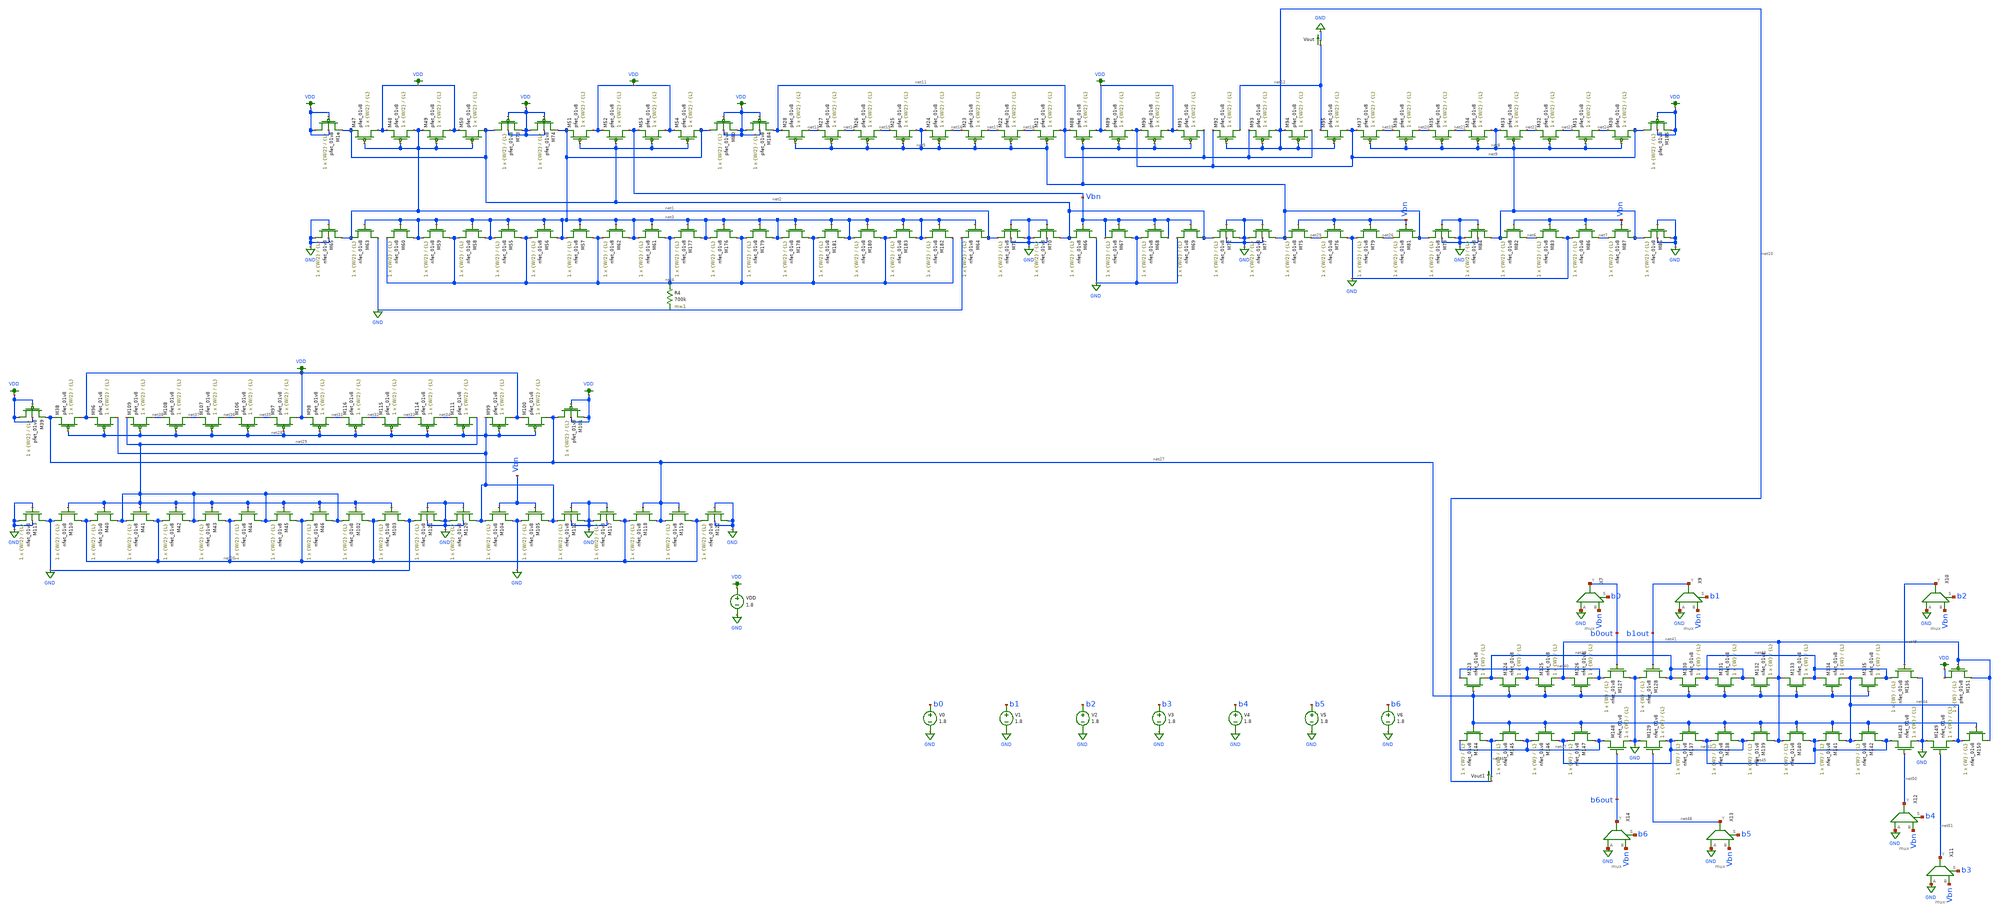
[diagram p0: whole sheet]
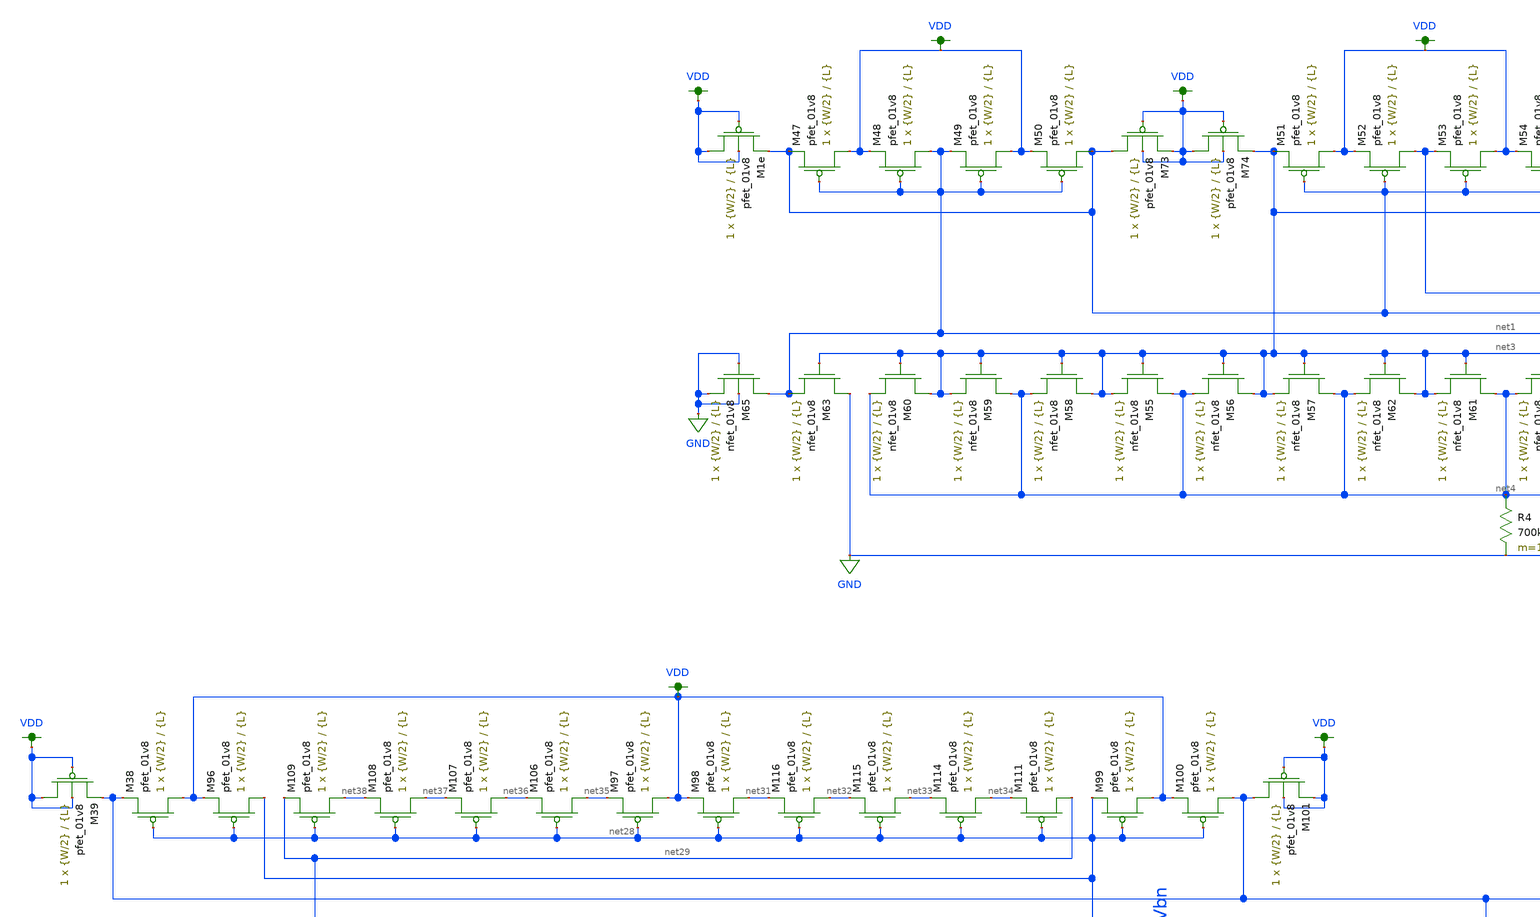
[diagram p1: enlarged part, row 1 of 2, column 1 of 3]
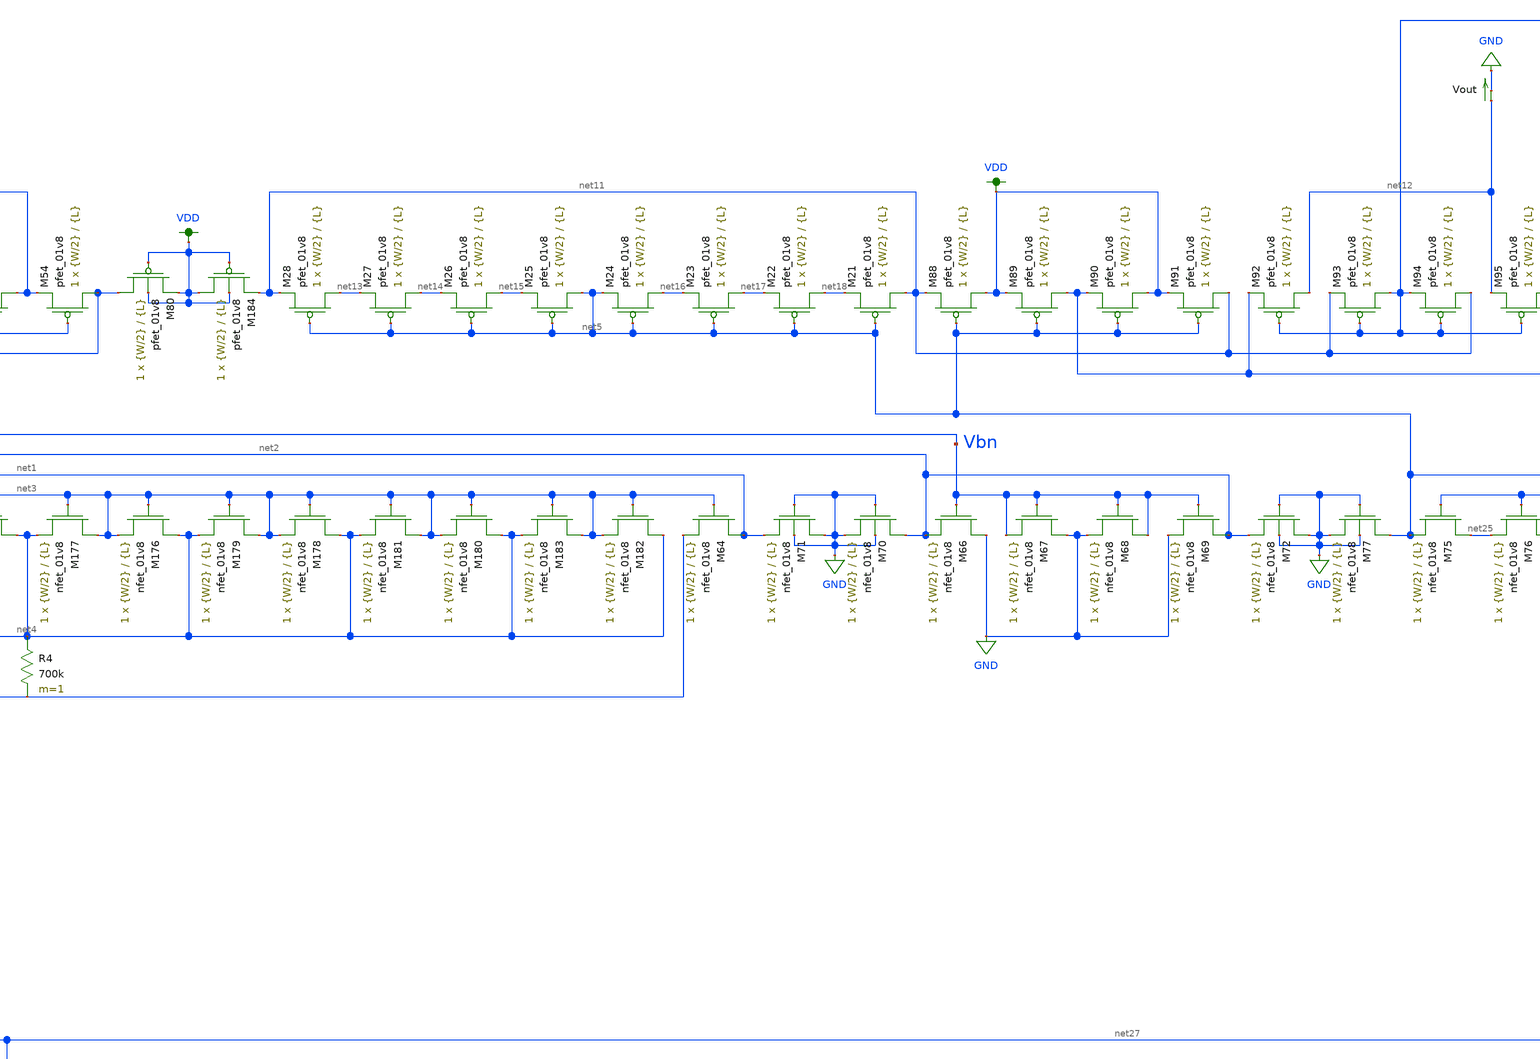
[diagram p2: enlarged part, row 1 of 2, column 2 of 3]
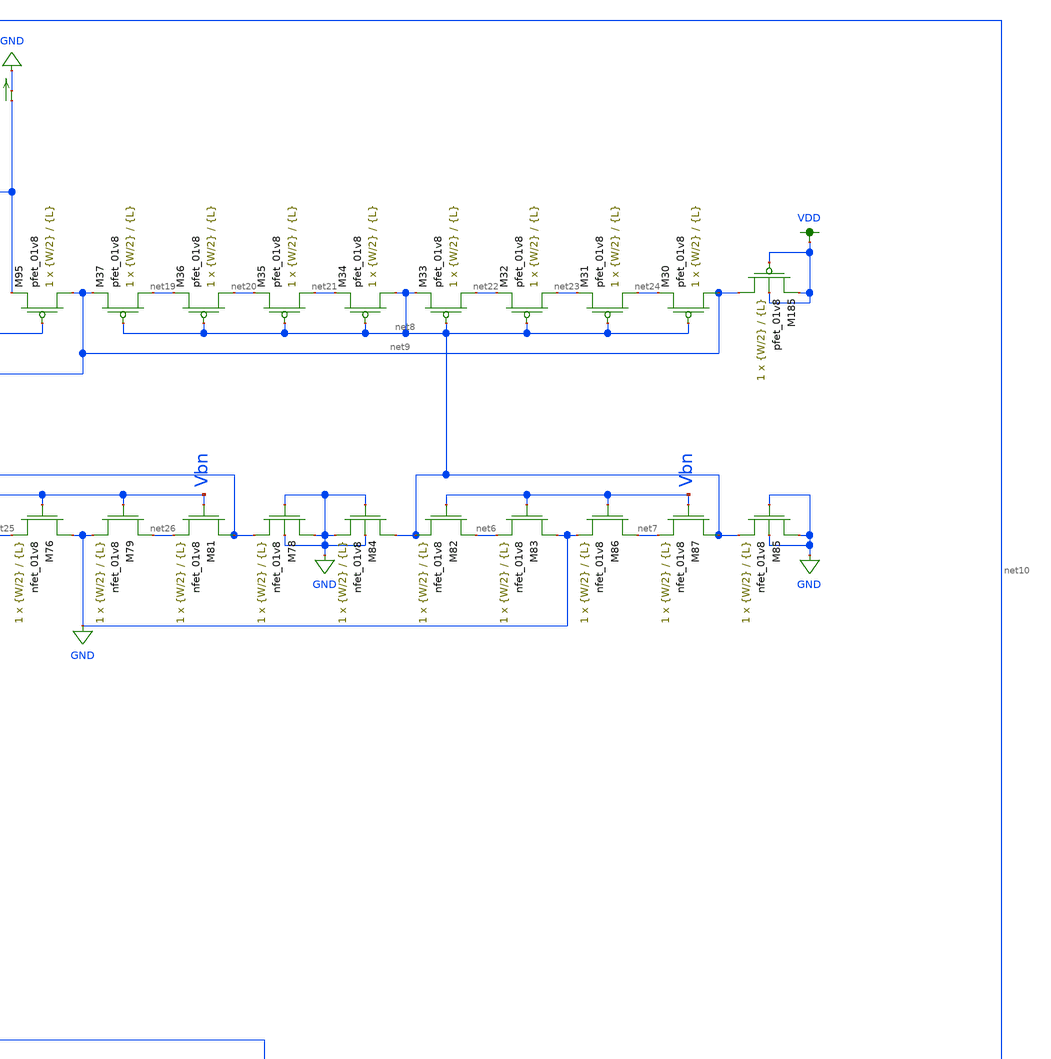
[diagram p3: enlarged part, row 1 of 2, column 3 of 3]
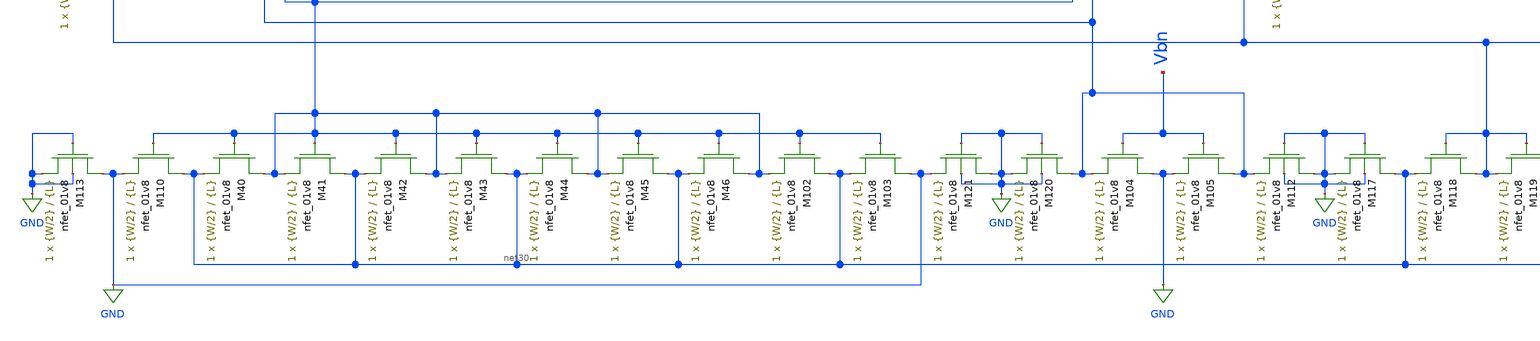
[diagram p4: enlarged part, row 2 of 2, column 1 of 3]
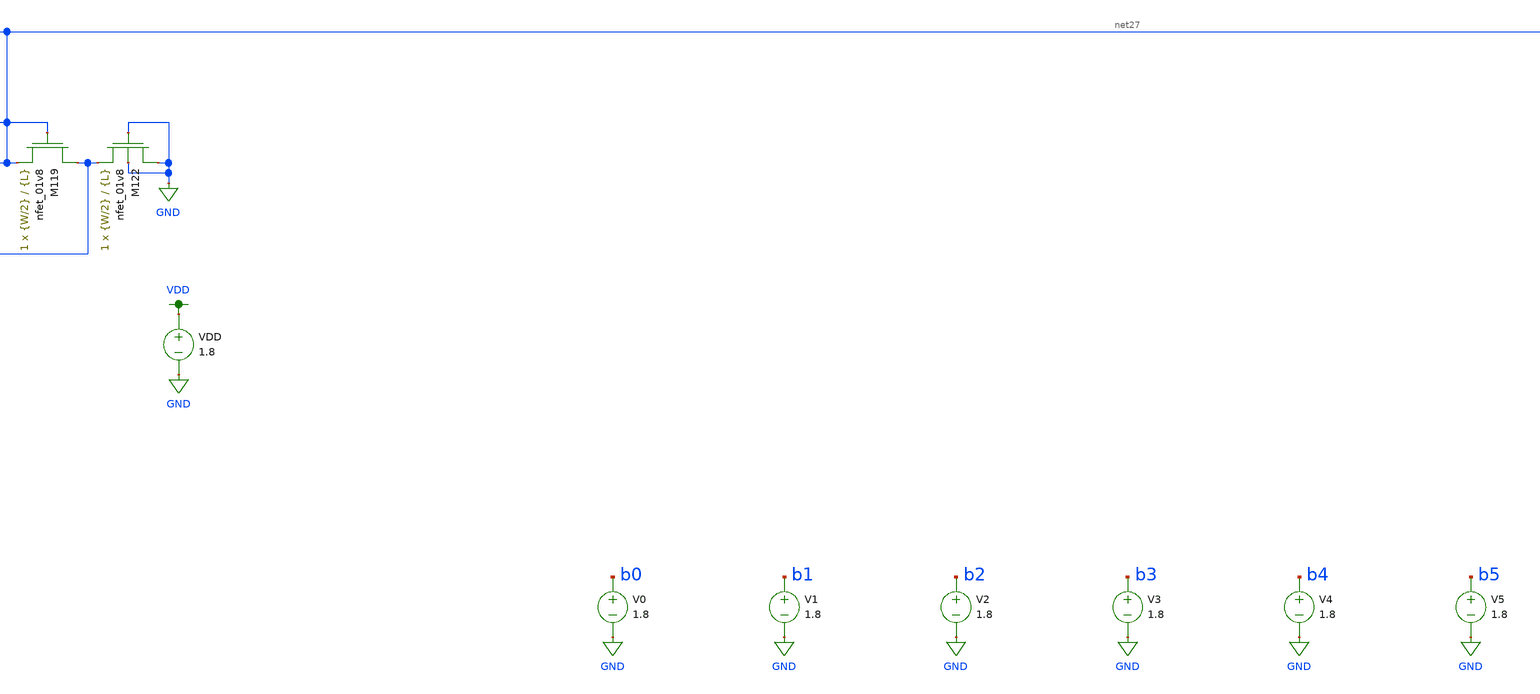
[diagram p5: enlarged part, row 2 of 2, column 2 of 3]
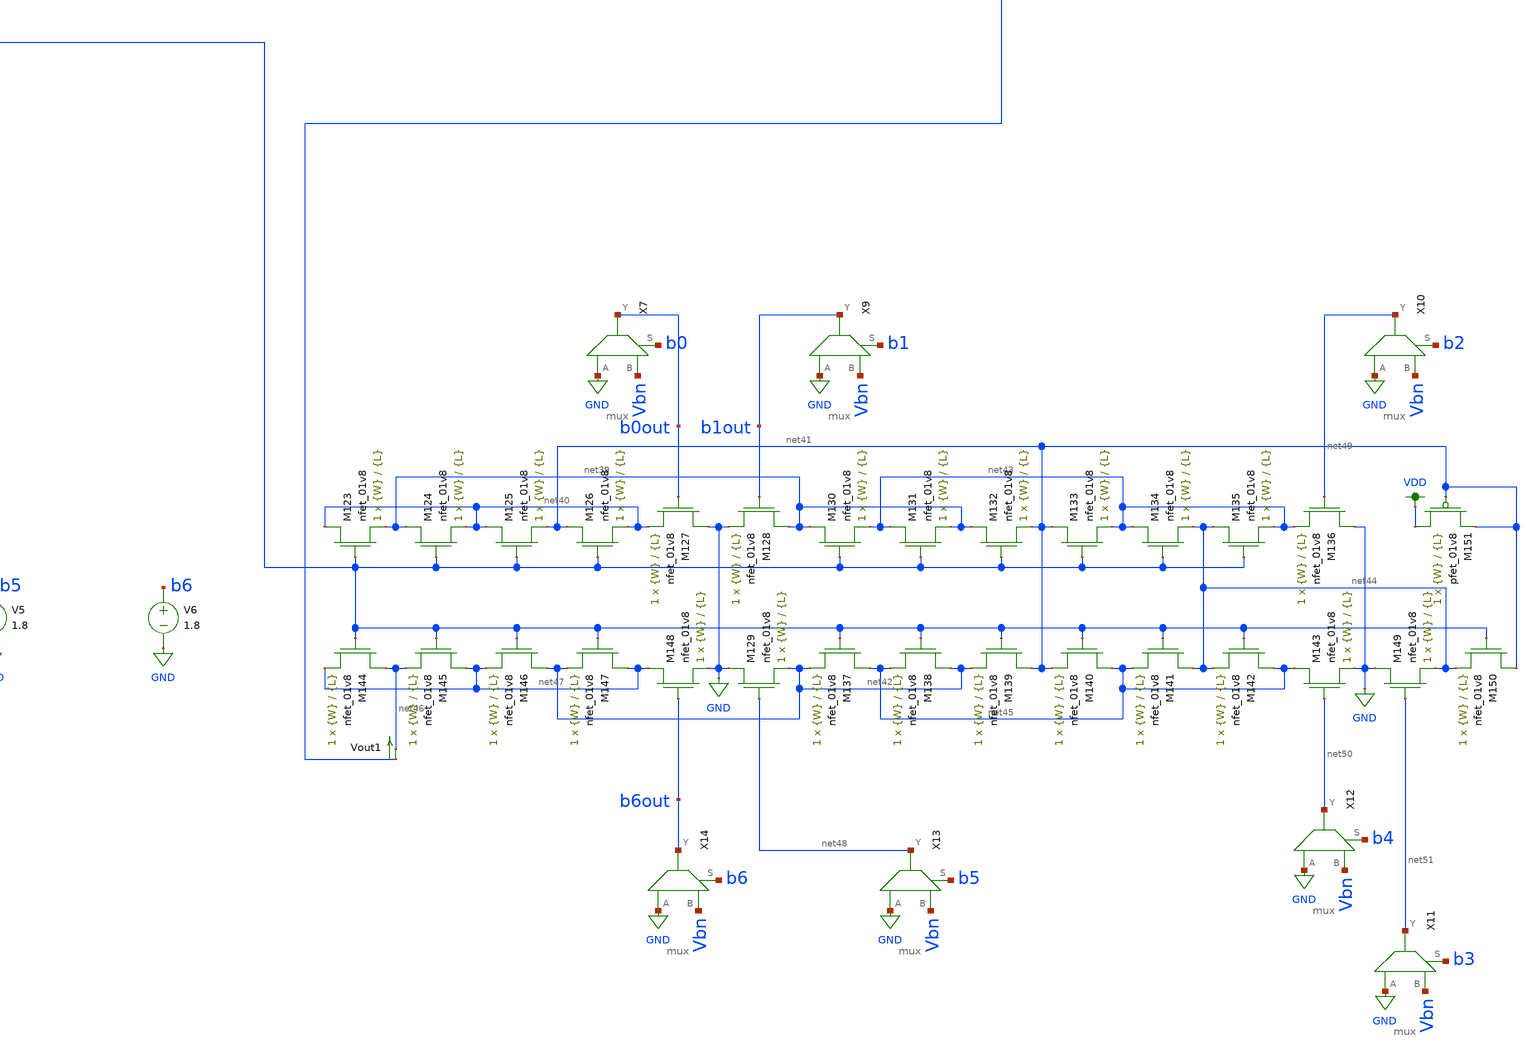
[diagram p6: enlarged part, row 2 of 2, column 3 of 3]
** sch_path: schematics/dac_dnl_inl_current_mirror_lds.sch
**.subckt dac_dnl_inl_current_mirror_lds
V0 b0 GND 1.8
V1 b1 GND 1.8
V2 b2 GND 1.8
V3 b3 GND 1.8
V4 b4 GND 1.8
V5 b5 GND 1.8
V6 b6 GND 1.8
VDD VDD GND 1.8
XM47 VDD net1 net2 VDD sky130_fd_pr__pfet_01v8 L={L} W={W/2} nf=1 ad='int((nf+1)/2) * W/nf * 0.29' as='int((nf+2)/2) * W/nf * 0.29'
+ pd='2*int((nf+1)/2) * (W/nf + 0.29)' ps='2*int((nf+2)/2) * (W/nf + 0.29)' nrd='0.29 / W' nrs='0.29 / W'
+ sa=0 sb=0 sd=0 mult=1 m=1
XM48 net1 net1 VDD VDD sky130_fd_pr__pfet_01v8 L={L} W={W/2} nf=1 ad='int((nf+1)/2) * W/nf * 0.29' as='int((nf+2)/2) * W/nf * 0.29'
+ pd='2*int((nf+1)/2) * (W/nf + 0.29)' ps='2*int((nf+2)/2) * (W/nf + 0.29)' nrd='0.29 / W' nrs='0.29 / W'
+ sa=0 sb=0 sd=0 mult=1 m=1
XM49 VDD net1 net1 VDD sky130_fd_pr__pfet_01v8 L={L} W={W/2} nf=1 ad='int((nf+1)/2) * W/nf * 0.29' as='int((nf+2)/2) * W/nf * 0.29'
+ pd='2*int((nf+1)/2) * (W/nf + 0.29)' ps='2*int((nf+2)/2) * (W/nf + 0.29)' nrd='0.29 / W' nrs='0.29 / W'
+ sa=0 sb=0 sd=0 mult=1 m=1
XM50 net2 net1 VDD VDD sky130_fd_pr__pfet_01v8 L={L} W={W/2} nf=1 ad='int((nf+1)/2) * W/nf * 0.29' as='int((nf+2)/2) * W/nf * 0.29'
+ pd='2*int((nf+1)/2) * (W/nf + 0.29)' ps='2*int((nf+2)/2) * (W/nf + 0.29)' nrd='0.29 / W' nrs='0.29 / W'
+ sa=0 sb=0 sd=0 mult=1 m=1
XM51 VDD net2 net3 VDD sky130_fd_pr__pfet_01v8 L={L} W={W/2} nf=1 ad='int((nf+1)/2) * W/nf * 0.29' as='int((nf+2)/2) * W/nf * 0.29'
+ pd='2*int((nf+1)/2) * (W/nf + 0.29)' ps='2*int((nf+2)/2) * (W/nf + 0.29)' nrd='0.29 / W' nrs='0.29 / W'
+ sa=0 sb=0 sd=0 mult=1 m=1
XM52 Vbn net2 VDD VDD sky130_fd_pr__pfet_01v8 L={L} W={W/2} nf=1 ad='int((nf+1)/2) * W/nf * 0.29' as='int((nf+2)/2) * W/nf * 0.29'
+ pd='2*int((nf+1)/2) * (W/nf + 0.29)' ps='2*int((nf+2)/2) * (W/nf + 0.29)' nrd='0.29 / W' nrs='0.29 / W'
+ sa=0 sb=0 sd=0 mult=1 m=1
XM53 VDD net2 Vbn VDD sky130_fd_pr__pfet_01v8 L={L} W={W/2} nf=1 ad='int((nf+1)/2) * W/nf * 0.29' as='int((nf+2)/2) * W/nf * 0.29'
+ pd='2*int((nf+1)/2) * (W/nf + 0.29)' ps='2*int((nf+2)/2) * (W/nf + 0.29)' nrd='0.29 / W' nrs='0.29 / W'
+ sa=0 sb=0 sd=0 mult=1 m=1
XM54 net3 net2 VDD VDD sky130_fd_pr__pfet_01v8 L={L} W={W/2} nf=1 ad='int((nf+1)/2) * W/nf * 0.29' as='int((nf+2)/2) * W/nf * 0.29'
+ pd='2*int((nf+1)/2) * (W/nf + 0.29)' ps='2*int((nf+2)/2) * (W/nf + 0.29)' nrd='0.29 / W' nrs='0.29 / W'
+ sa=0 sb=0 sd=0 mult=1 m=1
XM55 net4 net3 net3 GND sky130_fd_pr__nfet_01v8 L={L} W={W/2} nf=1 ad='int((nf+1)/2) * W/nf * 0.29' as='int((nf+2)/2) * W/nf * 0.29'
+ pd='2*int((nf+1)/2) * (W/nf + 0.29)' ps='2*int((nf+2)/2) * (W/nf + 0.29)' nrd='0.29 / W' nrs='0.29 / W'
+ sa=0 sb=0 sd=0 mult=1 m=1
XM56 net3 net3 net4 GND sky130_fd_pr__nfet_01v8 L={L} W={W/2} nf=1 ad='int((nf+1)/2) * W/nf * 0.29' as='int((nf+2)/2) * W/nf * 0.29'
+ pd='2*int((nf+1)/2) * (W/nf + 0.29)' ps='2*int((nf+2)/2) * (W/nf + 0.29)' nrd='0.29 / W' nrs='0.29 / W'
+ sa=0 sb=0 sd=0 mult=1 m=1
XM57 net4 net3 net3 GND sky130_fd_pr__nfet_01v8 L={L} W={W/2} nf=1 ad='int((nf+1)/2) * W/nf * 0.29' as='int((nf+2)/2) * W/nf * 0.29'
+ pd='2*int((nf+1)/2) * (W/nf + 0.29)' ps='2*int((nf+2)/2) * (W/nf + 0.29)' nrd='0.29 / W' nrs='0.29 / W'
+ sa=0 sb=0 sd=0 mult=1 m=1
XM58 net3 net3 net4 GND sky130_fd_pr__nfet_01v8 L={L} W={W/2} nf=1 ad='int((nf+1)/2) * W/nf * 0.29' as='int((nf+2)/2) * W/nf * 0.29'
+ pd='2*int((nf+1)/2) * (W/nf + 0.29)' ps='2*int((nf+2)/2) * (W/nf + 0.29)' nrd='0.29 / W' nrs='0.29 / W'
+ sa=0 sb=0 sd=0 mult=1 m=1
XM59 net4 net3 net3 GND sky130_fd_pr__nfet_01v8 L={L} W={W/2} nf=1 ad='int((nf+1)/2) * W/nf * 0.29' as='int((nf+2)/2) * W/nf * 0.29'
+ pd='2*int((nf+1)/2) * (W/nf + 0.29)' ps='2*int((nf+2)/2) * (W/nf + 0.29)' nrd='0.29 / W' nrs='0.29 / W'
+ sa=0 sb=0 sd=0 mult=1 m=1
XM60 net3 net3 net4 GND sky130_fd_pr__nfet_01v8 L={L} W={W/2} nf=1 ad='int((nf+1)/2) * W/nf * 0.29' as='int((nf+2)/2) * W/nf * 0.29'
+ pd='2*int((nf+1)/2) * (W/nf + 0.29)' ps='2*int((nf+2)/2) * (W/nf + 0.29)' nrd='0.29 / W' nrs='0.29 / W'
+ sa=0 sb=0 sd=0 mult=1 m=1
XM61 net4 net3 net3 GND sky130_fd_pr__nfet_01v8 L={L} W={W/2} nf=1 ad='int((nf+1)/2) * W/nf * 0.29' as='int((nf+2)/2) * W/nf * 0.29'
+ pd='2*int((nf+1)/2) * (W/nf + 0.29)' ps='2*int((nf+2)/2) * (W/nf + 0.29)' nrd='0.29 / W' nrs='0.29 / W'
+ sa=0 sb=0 sd=0 mult=1 m=1
XM62 net3 net3 net4 GND sky130_fd_pr__nfet_01v8 L={L} W={W/2} nf=1 ad='int((nf+1)/2) * W/nf * 0.29' as='int((nf+2)/2) * W/nf * 0.29'
+ pd='2*int((nf+1)/2) * (W/nf + 0.29)' ps='2*int((nf+2)/2) * (W/nf + 0.29)' nrd='0.29 / W' nrs='0.29 / W'
+ sa=0 sb=0 sd=0 mult=1 m=1
XM63 GND net3 net1 GND sky130_fd_pr__nfet_01v8 L={L} W={W/2} nf=1 ad='int((nf+1)/2) * W/nf * 0.29' as='int((nf+2)/2) * W/nf * 0.29'
+ pd='2*int((nf+1)/2) * (W/nf + 0.29)' ps='2*int((nf+2)/2) * (W/nf + 0.29)' nrd='0.29 / W' nrs='0.29 / W'
+ sa=0 sb=0 sd=0 mult=1 m=1
XM64 net1 net3 GND GND sky130_fd_pr__nfet_01v8 L={L} W={W/2} nf=1 ad='int((nf+1)/2) * W/nf * 0.29' as='int((nf+2)/2) * W/nf * 0.29'
+ pd='2*int((nf+1)/2) * (W/nf + 0.29)' ps='2*int((nf+2)/2) * (W/nf + 0.29)' nrd='0.29 / W' nrs='0.29 / W'
+ sa=0 sb=0 sd=0 mult=1 m=1
R4 net4 GND 700k m=1
XM1e VDD VDD net2 VDD sky130_fd_pr__pfet_01v8 L={L} W={W/2} nf=1 ad='int((nf+1)/2) * W/nf * 0.29' as='int((nf+2)/2) * W/nf * 0.29'
+ pd='2*int((nf+1)/2) * (W/nf + 0.29)' ps='2*int((nf+2)/2) * (W/nf + 0.29)' nrd='0.29 / W' nrs='0.29 / W'
+ sa=0 sb=0 sd=0 mult=1 m=1
XM65 net1 GND GND GND sky130_fd_pr__nfet_01v8 L={L} W={W/2} nf=1 ad='int((nf+1)/2) * W/nf * 0.29' as='int((nf+2)/2) * W/nf * 0.29'
+ pd='2*int((nf+1)/2) * (W/nf + 0.29)' ps='2*int((nf+2)/2) * (W/nf + 0.29)' nrd='0.29 / W' nrs='0.29 / W'
+ sa=0 sb=0 sd=0 mult=1 m=1
XM66 GND Vbn net2 GND sky130_fd_pr__nfet_01v8 L={L} W={W/2} nf=1 ad='int((nf+1)/2) * W/nf * 0.29' as='int((nf+2)/2) * W/nf * 0.29'
+ pd='2*int((nf+1)/2) * (W/nf + 0.29)' ps='2*int((nf+2)/2) * (W/nf + 0.29)' nrd='0.29 / W' nrs='0.29 / W'
+ sa=0 sb=0 sd=0 mult=1 m=1
XM67 GND Vbn Vbn GND sky130_fd_pr__nfet_01v8 L={L} W={W/2} nf=1 ad='int((nf+1)/2) * W/nf * 0.29' as='int((nf+2)/2) * W/nf * 0.29'
+ pd='2*int((nf+1)/2) * (W/nf + 0.29)' ps='2*int((nf+2)/2) * (W/nf + 0.29)' nrd='0.29 / W' nrs='0.29 / W'
+ sa=0 sb=0 sd=0 mult=1 m=1
XM68 Vbn Vbn GND GND sky130_fd_pr__nfet_01v8 L={L} W={W/2} nf=1 ad='int((nf+1)/2) * W/nf * 0.29' as='int((nf+2)/2) * W/nf * 0.29'
+ pd='2*int((nf+1)/2) * (W/nf + 0.29)' ps='2*int((nf+2)/2) * (W/nf + 0.29)' nrd='0.29 / W' nrs='0.29 / W'
+ sa=0 sb=0 sd=0 mult=1 m=1
XM69 net2 Vbn GND GND sky130_fd_pr__nfet_01v8 L={L} W={W/2} nf=1 ad='int((nf+1)/2) * W/nf * 0.29' as='int((nf+2)/2) * W/nf * 0.29'
+ pd='2*int((nf+1)/2) * (W/nf + 0.29)' ps='2*int((nf+2)/2) * (W/nf + 0.29)' nrd='0.29 / W' nrs='0.29 / W'
+ sa=0 sb=0 sd=0 mult=1 m=1
XM70 net2 GND GND GND sky130_fd_pr__nfet_01v8 L={L} W={W/2} nf=1 ad='int((nf+1)/2) * W/nf * 0.29' as='int((nf+2)/2) * W/nf * 0.29'
+ pd='2*int((nf+1)/2) * (W/nf + 0.29)' ps='2*int((nf+2)/2) * (W/nf + 0.29)' nrd='0.29 / W' nrs='0.29 / W'
+ sa=0 sb=0 sd=0 mult=1 m=1
XM71 GND GND net1 GND sky130_fd_pr__nfet_01v8 L={L} W={W/2} nf=1 ad='int((nf+1)/2) * W/nf * 0.29' as='int((nf+2)/2) * W/nf * 0.29'
+ pd='2*int((nf+1)/2) * (W/nf + 0.29)' ps='2*int((nf+2)/2) * (W/nf + 0.29)' nrd='0.29 / W' nrs='0.29 / W'
+ sa=0 sb=0 sd=0 mult=1 m=1
XM72 GND GND net2 GND sky130_fd_pr__nfet_01v8 L={L} W={W/2} nf=1 ad='int((nf+1)/2) * W/nf * 0.29' as='int((nf+2)/2) * W/nf * 0.29'
+ pd='2*int((nf+1)/2) * (W/nf + 0.29)' ps='2*int((nf+2)/2) * (W/nf + 0.29)' nrd='0.29 / W' nrs='0.29 / W'
+ sa=0 sb=0 sd=0 mult=1 m=1
XM77 net5 GND GND GND sky130_fd_pr__nfet_01v8 L={L} W={W/2} nf=1 ad='int((nf+1)/2) * W/nf * 0.29' as='int((nf+2)/2) * W/nf * 0.29'
+ pd='2*int((nf+1)/2) * (W/nf + 0.29)' ps='2*int((nf+2)/2) * (W/nf + 0.29)' nrd='0.29 / W' nrs='0.29 / W'
+ sa=0 sb=0 sd=0 mult=1 m=1
XM78 GND GND net5 GND sky130_fd_pr__nfet_01v8 L={L} W={W/2} nf=1 ad='int((nf+1)/2) * W/nf * 0.29' as='int((nf+2)/2) * W/nf * 0.29'
+ pd='2*int((nf+1)/2) * (W/nf + 0.29)' ps='2*int((nf+2)/2) * (W/nf + 0.29)' nrd='0.29 / W' nrs='0.29 / W'
+ sa=0 sb=0 sd=0 mult=1 m=1
XM73 net2 VDD VDD VDD sky130_fd_pr__pfet_01v8 L={L} W={W/2} nf=1 ad='int((nf+1)/2) * W/nf * 0.29' as='int((nf+2)/2) * W/nf * 0.29'
+ pd='2*int((nf+1)/2) * (W/nf + 0.29)' ps='2*int((nf+2)/2) * (W/nf + 0.29)' nrd='0.29 / W' nrs='0.29 / W'
+ sa=0 sb=0 sd=0 mult=1 m=1
XM74 VDD VDD net3 VDD sky130_fd_pr__pfet_01v8 L={L} W={W/2} nf=1 ad='int((nf+1)/2) * W/nf * 0.29' as='int((nf+2)/2) * W/nf * 0.29'
+ pd='2*int((nf+1)/2) * (W/nf + 0.29)' ps='2*int((nf+2)/2) * (W/nf + 0.29)' nrd='0.29 / W' nrs='0.29 / W'
+ sa=0 sb=0 sd=0 mult=1 m=1
XM80 net3 VDD VDD VDD sky130_fd_pr__pfet_01v8 L={L} W={W/2} nf=1 ad='int((nf+1)/2) * W/nf * 0.29' as='int((nf+2)/2) * W/nf * 0.29'
+ pd='2*int((nf+1)/2) * (W/nf + 0.29)' ps='2*int((nf+2)/2) * (W/nf + 0.29)' nrd='0.29 / W' nrs='0.29 / W'
+ sa=0 sb=0 sd=0 mult=1 m=1
XM84 net8 GND GND GND sky130_fd_pr__nfet_01v8 L={L} W={W/2} nf=1 ad='int((nf+1)/2) * W/nf * 0.29' as='int((nf+2)/2) * W/nf * 0.29'
+ pd='2*int((nf+1)/2) * (W/nf + 0.29)' ps='2*int((nf+2)/2) * (W/nf + 0.29)' nrd='0.29 / W' nrs='0.29 / W'
+ sa=0 sb=0 sd=0 mult=1 m=1
XM85 GND GND net8 GND sky130_fd_pr__nfet_01v8 L={L} W={W/2} nf=1 ad='int((nf+1)/2) * W/nf * 0.29' as='int((nf+2)/2) * W/nf * 0.29'
+ pd='2*int((nf+1)/2) * (W/nf + 0.29)' ps='2*int((nf+2)/2) * (W/nf + 0.29)' nrd='0.29 / W' nrs='0.29 / W'
+ sa=0 sb=0 sd=0 mult=1 m=1
XM75 net25 Vbn net5 GND sky130_fd_pr__nfet_01v8 L={L} W={W/2} nf=1 ad='int((nf+1)/2) * W/nf * 0.29' as='int((nf+2)/2) * W/nf * 0.29'
+ pd='2*int((nf+1)/2) * (W/nf + 0.29)' ps='2*int((nf+2)/2) * (W/nf + 0.29)' nrd='0.29 / W' nrs='0.29 / W'
+ sa=0 sb=0 sd=0 mult=1 m=1
XM76 GND Vbn net25 GND sky130_fd_pr__nfet_01v8 L={L} W={W/2} nf=1 ad='int((nf+1)/2) * W/nf * 0.29' as='int((nf+2)/2) * W/nf * 0.29'
+ pd='2*int((nf+1)/2) * (W/nf + 0.29)' ps='2*int((nf+2)/2) * (W/nf + 0.29)' nrd='0.29 / W' nrs='0.29 / W'
+ sa=0 sb=0 sd=0 mult=1 m=1
XM79 net26 Vbn GND GND sky130_fd_pr__nfet_01v8 L={L} W={W/2} nf=1 ad='int((nf+1)/2) * W/nf * 0.29' as='int((nf+2)/2) * W/nf * 0.29'
+ pd='2*int((nf+1)/2) * (W/nf + 0.29)' ps='2*int((nf+2)/2) * (W/nf + 0.29)' nrd='0.29 / W' nrs='0.29 / W'
+ sa=0 sb=0 sd=0 mult=1 m=1
XM81 net5 Vbn net26 GND sky130_fd_pr__nfet_01v8 L={L} W={W/2} nf=1 ad='int((nf+1)/2) * W/nf * 0.29' as='int((nf+2)/2) * W/nf * 0.29'
+ pd='2*int((nf+1)/2) * (W/nf + 0.29)' ps='2*int((nf+2)/2) * (W/nf + 0.29)' nrd='0.29 / W' nrs='0.29 / W'
+ sa=0 sb=0 sd=0 mult=1 m=1
XM82 net6 Vbn net8 GND sky130_fd_pr__nfet_01v8 L={L} W={W/2} nf=1 ad='int((nf+1)/2) * W/nf * 0.29' as='int((nf+2)/2) * W/nf * 0.29'
+ pd='2*int((nf+1)/2) * (W/nf + 0.29)' ps='2*int((nf+2)/2) * (W/nf + 0.29)' nrd='0.29 / W' nrs='0.29 / W'
+ sa=0 sb=0 sd=0 mult=1 m=1
XM83 GND Vbn net6 GND sky130_fd_pr__nfet_01v8 L={L} W={W/2} nf=1 ad='int((nf+1)/2) * W/nf * 0.29' as='int((nf+2)/2) * W/nf * 0.29'
+ pd='2*int((nf+1)/2) * (W/nf + 0.29)' ps='2*int((nf+2)/2) * (W/nf + 0.29)' nrd='0.29 / W' nrs='0.29 / W'
+ sa=0 sb=0 sd=0 mult=1 m=1
XM86 net7 Vbn GND GND sky130_fd_pr__nfet_01v8 L={L} W={W/2} nf=1 ad='int((nf+1)/2) * W/nf * 0.29' as='int((nf+2)/2) * W/nf * 0.29'
+ pd='2*int((nf+1)/2) * (W/nf + 0.29)' ps='2*int((nf+2)/2) * (W/nf + 0.29)' nrd='0.29 / W' nrs='0.29 / W'
+ sa=0 sb=0 sd=0 mult=1 m=1
XM87 net8 Vbn net7 GND sky130_fd_pr__nfet_01v8 L={L} W={W/2} nf=1 ad='int((nf+1)/2) * W/nf * 0.29' as='int((nf+2)/2) * W/nf * 0.29'
+ pd='2*int((nf+1)/2) * (W/nf + 0.29)' ps='2*int((nf+2)/2) * (W/nf + 0.29)' nrd='0.29 / W' nrs='0.29 / W'
+ sa=0 sb=0 sd=0 mult=1 m=1
XM88 VDD net5 net11 VDD sky130_fd_pr__pfet_01v8 L={L} W={W/2} nf=1 ad='int((nf+1)/2) * W/nf * 0.29' as='int((nf+2)/2) * W/nf * 0.29'
+ pd='2*int((nf+1)/2) * (W/nf + 0.29)' ps='2*int((nf+2)/2) * (W/nf + 0.29)' nrd='0.29 / W' nrs='0.29 / W'
+ sa=0 sb=0 sd=0 mult=1 m=1
XM89 net9 net5 VDD VDD sky130_fd_pr__pfet_01v8 L={L} W={W/2} nf=1 ad='int((nf+1)/2) * W/nf * 0.29' as='int((nf+2)/2) * W/nf * 0.29'
+ pd='2*int((nf+1)/2) * (W/nf + 0.29)' ps='2*int((nf+2)/2) * (W/nf + 0.29)' nrd='0.29 / W' nrs='0.29 / W'
+ sa=0 sb=0 sd=0 mult=1 m=1
XM90 VDD net5 net9 VDD sky130_fd_pr__pfet_01v8 L={L} W={W/2} nf=1 ad='int((nf+1)/2) * W/nf * 0.29' as='int((nf+2)/2) * W/nf * 0.29'
+ pd='2*int((nf+1)/2) * (W/nf + 0.29)' ps='2*int((nf+2)/2) * (W/nf + 0.29)' nrd='0.29 / W' nrs='0.29 / W'
+ sa=0 sb=0 sd=0 mult=1 m=1
XM91 net11 net5 VDD VDD sky130_fd_pr__pfet_01v8 L={L} W={W/2} nf=1 ad='int((nf+1)/2) * W/nf * 0.29' as='int((nf+2)/2) * W/nf * 0.29'
+ pd='2*int((nf+1)/2) * (W/nf + 0.29)' ps='2*int((nf+2)/2) * (W/nf + 0.29)' nrd='0.29 / W' nrs='0.29 / W'
+ sa=0 sb=0 sd=0 mult=1 m=1
XM92 net12 net10 net9 VDD sky130_fd_pr__pfet_01v8 L={L} W={W/2} nf=1 ad='int((nf+1)/2) * W/nf * 0.29'
+ as='int((nf+2)/2) * W/nf * 0.29' pd='2*int((nf+1)/2) * (W/nf + 0.29)' ps='2*int((nf+2)/2) * (W/nf + 0.29)'
+ nrd='0.29 / W' nrs='0.29 / W' sa=0 sb=0 sd=0 mult=1 m=1
XM93 net10 net10 net11 VDD sky130_fd_pr__pfet_01v8 L={L} W={W/2} nf=1 ad='int((nf+1)/2) * W/nf * 0.29'
+ as='int((nf+2)/2) * W/nf * 0.29' pd='2*int((nf+1)/2) * (W/nf + 0.29)' ps='2*int((nf+2)/2) * (W/nf + 0.29)'
+ nrd='0.29 / W' nrs='0.29 / W' sa=0 sb=0 sd=0 mult=1 m=1
XM94 net11 net10 net10 VDD sky130_fd_pr__pfet_01v8 L={L} W={W/2} nf=1 ad='int((nf+1)/2) * W/nf * 0.29'
+ as='int((nf+2)/2) * W/nf * 0.29' pd='2*int((nf+1)/2) * (W/nf + 0.29)' ps='2*int((nf+2)/2) * (W/nf + 0.29)'
+ nrd='0.29 / W' nrs='0.29 / W' sa=0 sb=0 sd=0 mult=1 m=1
XM95 net9 net10 net12 VDD sky130_fd_pr__pfet_01v8 L={L} W={W/2} nf=1 ad='int((nf+1)/2) * W/nf * 0.29'
+ as='int((nf+2)/2) * W/nf * 0.29' pd='2*int((nf+1)/2) * (W/nf + 0.29)' ps='2*int((nf+2)/2) * (W/nf + 0.29)'
+ nrd='0.29 / W' nrs='0.29 / W' sa=0 sb=0 sd=0 mult=1 m=1
XM176 net4 net3 net3 GND sky130_fd_pr__nfet_01v8 L={L} W={W/2} nf=1 ad='int((nf+1)/2) * W/nf * 0.29'
+ as='int((nf+2)/2) * W/nf * 0.29' pd='2*int((nf+1)/2) * (W/nf + 0.29)' ps='2*int((nf+2)/2) * (W/nf + 0.29)'
+ nrd='0.29 / W' nrs='0.29 / W' sa=0 sb=0 sd=0 mult=1 m=1
XM177 net3 net3 net4 GND sky130_fd_pr__nfet_01v8 L={L} W={W/2} nf=1 ad='int((nf+1)/2) * W/nf * 0.29'
+ as='int((nf+2)/2) * W/nf * 0.29' pd='2*int((nf+1)/2) * (W/nf + 0.29)' ps='2*int((nf+2)/2) * (W/nf + 0.29)'
+ nrd='0.29 / W' nrs='0.29 / W' sa=0 sb=0 sd=0 mult=1 m=1
XM178 net4 net3 net3 GND sky130_fd_pr__nfet_01v8 L={L} W={W/2} nf=1 ad='int((nf+1)/2) * W/nf * 0.29'
+ as='int((nf+2)/2) * W/nf * 0.29' pd='2*int((nf+1)/2) * (W/nf + 0.29)' ps='2*int((nf+2)/2) * (W/nf + 0.29)'
+ nrd='0.29 / W' nrs='0.29 / W' sa=0 sb=0 sd=0 mult=1 m=1
XM179 net3 net3 net4 GND sky130_fd_pr__nfet_01v8 L={L} W={W/2} nf=1 ad='int((nf+1)/2) * W/nf * 0.29'
+ as='int((nf+2)/2) * W/nf * 0.29' pd='2*int((nf+1)/2) * (W/nf + 0.29)' ps='2*int((nf+2)/2) * (W/nf + 0.29)'
+ nrd='0.29 / W' nrs='0.29 / W' sa=0 sb=0 sd=0 mult=1 m=1
XM180 net4 net3 net3 GND sky130_fd_pr__nfet_01v8 L={L} W={W/2} nf=1 ad='int((nf+1)/2) * W/nf * 0.29'
+ as='int((nf+2)/2) * W/nf * 0.29' pd='2*int((nf+1)/2) * (W/nf + 0.29)' ps='2*int((nf+2)/2) * (W/nf + 0.29)'
+ nrd='0.29 / W' nrs='0.29 / W' sa=0 sb=0 sd=0 mult=1 m=1
XM181 net3 net3 net4 GND sky130_fd_pr__nfet_01v8 L={L} W={W/2} nf=1 ad='int((nf+1)/2) * W/nf * 0.29'
+ as='int((nf+2)/2) * W/nf * 0.29' pd='2*int((nf+1)/2) * (W/nf + 0.29)' ps='2*int((nf+2)/2) * (W/nf + 0.29)'
+ nrd='0.29 / W' nrs='0.29 / W' sa=0 sb=0 sd=0 mult=1 m=1
XM182 net4 net3 net3 GND sky130_fd_pr__nfet_01v8 L={L} W={W/2} nf=1 ad='int((nf+1)/2) * W/nf * 0.29'
+ as='int((nf+2)/2) * W/nf * 0.29' pd='2*int((nf+1)/2) * (W/nf + 0.29)' ps='2*int((nf+2)/2) * (W/nf + 0.29)'
+ nrd='0.29 / W' nrs='0.29 / W' sa=0 sb=0 sd=0 mult=1 m=1
XM183 net3 net3 net4 GND sky130_fd_pr__nfet_01v8 L={L} W={W/2} nf=1 ad='int((nf+1)/2) * W/nf * 0.29'
+ as='int((nf+2)/2) * W/nf * 0.29' pd='2*int((nf+1)/2) * (W/nf + 0.29)' ps='2*int((nf+2)/2) * (W/nf + 0.29)'
+ nrd='0.29 / W' nrs='0.29 / W' sa=0 sb=0 sd=0 mult=1 m=1
XM184 VDD VDD net11 VDD sky130_fd_pr__pfet_01v8 L={L} W={W/2} nf=1 ad='int((nf+1)/2) * W/nf * 0.29' as='int((nf+2)/2) * W/nf * 0.29'
+ pd='2*int((nf+1)/2) * (W/nf + 0.29)' ps='2*int((nf+2)/2) * (W/nf + 0.29)' nrd='0.29 / W' nrs='0.29 / W'
+ sa=0 sb=0 sd=0 mult=1 m=1
XM185 net9 VDD VDD VDD sky130_fd_pr__pfet_01v8 L={L} W={W/2} nf=1 ad='int((nf+1)/2) * W/nf * 0.29' as='int((nf+2)/2) * W/nf * 0.29'
+ pd='2*int((nf+1)/2) * (W/nf + 0.29)' ps='2*int((nf+2)/2) * (W/nf + 0.29)' nrd='0.29 / W' nrs='0.29 / W'
+ sa=0 sb=0 sd=0 mult=1 m=1
Vout net12 GND 0
.save i(vout)
XM21 net11 net5 net18 VDD sky130_fd_pr__pfet_01v8 L={L} W={W/2} nf=1 ad='int((nf+1)/2) * W/nf * 0.29'
+ as='int((nf+2)/2) * W/nf * 0.29' pd='2*int((nf+1)/2) * (W/nf + 0.29)' ps='2*int((nf+2)/2) * (W/nf + 0.29)'
+ nrd='0.29 / W' nrs='0.29 / W' sa=0 sb=0 sd=0 mult=1 m=1
XM22 net18 net5 net17 VDD sky130_fd_pr__pfet_01v8 L={L} W={W/2} nf=1 ad='int((nf+1)/2) * W/nf * 0.29'
+ as='int((nf+2)/2) * W/nf * 0.29' pd='2*int((nf+1)/2) * (W/nf + 0.29)' ps='2*int((nf+2)/2) * (W/nf + 0.29)'
+ nrd='0.29 / W' nrs='0.29 / W' sa=0 sb=0 sd=0 mult=1 m=1
XM23 net17 net5 net16 VDD sky130_fd_pr__pfet_01v8 L={L} W={W/2} nf=1 ad='int((nf+1)/2) * W/nf * 0.29'
+ as='int((nf+2)/2) * W/nf * 0.29' pd='2*int((nf+1)/2) * (W/nf + 0.29)' ps='2*int((nf+2)/2) * (W/nf + 0.29)'
+ nrd='0.29 / W' nrs='0.29 / W' sa=0 sb=0 sd=0 mult=1 m=1
XM24 net16 net5 net5 VDD sky130_fd_pr__pfet_01v8 L={L} W={W/2} nf=1 ad='int((nf+1)/2) * W/nf * 0.29'
+ as='int((nf+2)/2) * W/nf * 0.29' pd='2*int((nf+1)/2) * (W/nf + 0.29)' ps='2*int((nf+2)/2) * (W/nf + 0.29)'
+ nrd='0.29 / W' nrs='0.29 / W' sa=0 sb=0 sd=0 mult=1 m=1
XM25 net5 net5 net15 VDD sky130_fd_pr__pfet_01v8 L={L} W={W/2} nf=1 ad='int((nf+1)/2) * W/nf * 0.29'
+ as='int((nf+2)/2) * W/nf * 0.29' pd='2*int((nf+1)/2) * (W/nf + 0.29)' ps='2*int((nf+2)/2) * (W/nf + 0.29)'
+ nrd='0.29 / W' nrs='0.29 / W' sa=0 sb=0 sd=0 mult=1 m=1
XM26 net15 net5 net14 VDD sky130_fd_pr__pfet_01v8 L={L} W={W/2} nf=1 ad='int((nf+1)/2) * W/nf * 0.29'
+ as='int((nf+2)/2) * W/nf * 0.29' pd='2*int((nf+1)/2) * (W/nf + 0.29)' ps='2*int((nf+2)/2) * (W/nf + 0.29)'
+ nrd='0.29 / W' nrs='0.29 / W' sa=0 sb=0 sd=0 mult=1 m=1
XM27 net14 net5 net13 VDD sky130_fd_pr__pfet_01v8 L={L} W={W/2} nf=1 ad='int((nf+1)/2) * W/nf * 0.29'
+ as='int((nf+2)/2) * W/nf * 0.29' pd='2*int((nf+1)/2) * (W/nf + 0.29)' ps='2*int((nf+2)/2) * (W/nf + 0.29)'
+ nrd='0.29 / W' nrs='0.29 / W' sa=0 sb=0 sd=0 mult=1 m=1
XM28 net13 net5 net11 VDD sky130_fd_pr__pfet_01v8 L={L} W={W/2} nf=1 ad='int((nf+1)/2) * W/nf * 0.29'
+ as='int((nf+2)/2) * W/nf * 0.29' pd='2*int((nf+1)/2) * (W/nf + 0.29)' ps='2*int((nf+2)/2) * (W/nf + 0.29)'
+ nrd='0.29 / W' nrs='0.29 / W' sa=0 sb=0 sd=0 mult=1 m=1
XM30 net9 net8 net24 VDD sky130_fd_pr__pfet_01v8 L={L} W={W/2} nf=1 ad='int((nf+1)/2) * W/nf * 0.29'
+ as='int((nf+2)/2) * W/nf * 0.29' pd='2*int((nf+1)/2) * (W/nf + 0.29)' ps='2*int((nf+2)/2) * (W/nf + 0.29)'
+ nrd='0.29 / W' nrs='0.29 / W' sa=0 sb=0 sd=0 mult=1 m=1
XM31 net24 net8 net23 VDD sky130_fd_pr__pfet_01v8 L={L} W={W/2} nf=1 ad='int((nf+1)/2) * W/nf * 0.29'
+ as='int((nf+2)/2) * W/nf * 0.29' pd='2*int((nf+1)/2) * (W/nf + 0.29)' ps='2*int((nf+2)/2) * (W/nf + 0.29)'
+ nrd='0.29 / W' nrs='0.29 / W' sa=0 sb=0 sd=0 mult=1 m=1
XM32 net23 net8 net22 VDD sky130_fd_pr__pfet_01v8 L={L} W={W/2} nf=1 ad='int((nf+1)/2) * W/nf * 0.29'
+ as='int((nf+2)/2) * W/nf * 0.29' pd='2*int((nf+1)/2) * (W/nf + 0.29)' ps='2*int((nf+2)/2) * (W/nf + 0.29)'
+ nrd='0.29 / W' nrs='0.29 / W' sa=0 sb=0 sd=0 mult=1 m=1
XM33 net22 net8 net8 VDD sky130_fd_pr__pfet_01v8 L={L} W={W/2} nf=1 ad='int((nf+1)/2) * W/nf * 0.29'
+ as='int((nf+2)/2) * W/nf * 0.29' pd='2*int((nf+1)/2) * (W/nf + 0.29)' ps='2*int((nf+2)/2) * (W/nf + 0.29)'
+ nrd='0.29 / W' nrs='0.29 / W' sa=0 sb=0 sd=0 mult=1 m=1
XM34 net8 net8 net21 VDD sky130_fd_pr__pfet_01v8 L={L} W={W/2} nf=1 ad='int((nf+1)/2) * W/nf * 0.29'
+ as='int((nf+2)/2) * W/nf * 0.29' pd='2*int((nf+1)/2) * (W/nf + 0.29)' ps='2*int((nf+2)/2) * (W/nf + 0.29)'
+ nrd='0.29 / W' nrs='0.29 / W' sa=0 sb=0 sd=0 mult=1 m=1
XM35 net21 net8 net20 VDD sky130_fd_pr__pfet_01v8 L={L} W={W/2} nf=1 ad='int((nf+1)/2) * W/nf * 0.29'
+ as='int((nf+2)/2) * W/nf * 0.29' pd='2*int((nf+1)/2) * (W/nf + 0.29)' ps='2*int((nf+2)/2) * (W/nf + 0.29)'
+ nrd='0.29 / W' nrs='0.29 / W' sa=0 sb=0 sd=0 mult=1 m=1
XM36 net20 net8 net19 VDD sky130_fd_pr__pfet_01v8 L={L} W={W/2} nf=1 ad='int((nf+1)/2) * W/nf * 0.29'
+ as='int((nf+2)/2) * W/nf * 0.29' pd='2*int((nf+1)/2) * (W/nf + 0.29)' ps='2*int((nf+2)/2) * (W/nf + 0.29)'
+ nrd='0.29 / W' nrs='0.29 / W' sa=0 sb=0 sd=0 mult=1 m=1
XM37 net19 net8 net9 VDD sky130_fd_pr__pfet_01v8 L={L} W={W/2} nf=1 ad='int((nf+1)/2) * W/nf * 0.29'
+ as='int((nf+2)/2) * W/nf * 0.29' pd='2*int((nf+1)/2) * (W/nf + 0.29)' ps='2*int((nf+2)/2) * (W/nf + 0.29)'
+ nrd='0.29 / W' nrs='0.29 / W' sa=0 sb=0 sd=0 mult=1 m=1
XM38 VDD net28 net27 VDD sky130_fd_pr__pfet_01v8 L={L} W={W/2} nf=1 ad='int((nf+1)/2) * W/nf * 0.29'
+ as='int((nf+2)/2) * W/nf * 0.29' pd='2*int((nf+1)/2) * (W/nf + 0.29)' ps='2*int((nf+2)/2) * (W/nf + 0.29)'
+ nrd='0.29 / W' nrs='0.29 / W' sa=0 sb=0 sd=0 mult=1 m=1
XM39 VDD VDD net27 VDD sky130_fd_pr__pfet_01v8 L={L} W={W/2} nf=1 ad='int((nf+1)/2) * W/nf * 0.29' as='int((nf+2)/2) * W/nf * 0.29'
+ pd='2*int((nf+1)/2) * (W/nf + 0.29)' ps='2*int((nf+2)/2) * (W/nf + 0.29)' nrd='0.29 / W' nrs='0.29 / W'
+ sa=0 sb=0 sd=0 mult=1 m=1
XM96 net28 net28 VDD VDD sky130_fd_pr__pfet_01v8 L={L} W={W/2} nf=1 ad='int((nf+1)/2) * W/nf * 0.29'
+ as='int((nf+2)/2) * W/nf * 0.29' pd='2*int((nf+1)/2) * (W/nf + 0.29)' ps='2*int((nf+2)/2) * (W/nf + 0.29)'
+ nrd='0.29 / W' nrs='0.29 / W' sa=0 sb=0 sd=0 mult=1 m=1
XM97 VDD net28 net35 VDD sky130_fd_pr__pfet_01v8 L={L} W={W/2} nf=1 ad='int((nf+1)/2) * W/nf * 0.29'
+ as='int((nf+2)/2) * W/nf * 0.29' pd='2*int((nf+1)/2) * (W/nf + 0.29)' ps='2*int((nf+2)/2) * (W/nf + 0.29)'
+ nrd='0.29 / W' nrs='0.29 / W' sa=0 sb=0 sd=0 mult=1 m=1
XM98 net31 net28 VDD VDD sky130_fd_pr__pfet_01v8 L={L} W={W/2} nf=1 ad='int((nf+1)/2) * W/nf * 0.29'
+ as='int((nf+2)/2) * W/nf * 0.29' pd='2*int((nf+1)/2) * (W/nf + 0.29)' ps='2*int((nf+2)/2) * (W/nf + 0.29)'
+ nrd='0.29 / W' nrs='0.29 / W' sa=0 sb=0 sd=0 mult=1 m=1
XM99 VDD net28 net28 VDD sky130_fd_pr__pfet_01v8 L={L} W={W/2} nf=1 ad='int((nf+1)/2) * W/nf * 0.29'
+ as='int((nf+2)/2) * W/nf * 0.29' pd='2*int((nf+1)/2) * (W/nf + 0.29)' ps='2*int((nf+2)/2) * (W/nf + 0.29)'
+ nrd='0.29 / W' nrs='0.29 / W' sa=0 sb=0 sd=0 mult=1 m=1
XM100 net27 net28 VDD VDD sky130_fd_pr__pfet_01v8 L={L} W={W/2} nf=1 ad='int((nf+1)/2) * W/nf * 0.29'
+ as='int((nf+2)/2) * W/nf * 0.29' pd='2*int((nf+1)/2) * (W/nf + 0.29)' ps='2*int((nf+2)/2) * (W/nf + 0.29)'
+ nrd='0.29 / W' nrs='0.29 / W' sa=0 sb=0 sd=0 mult=1 m=1
XM101 net27 VDD VDD VDD sky130_fd_pr__pfet_01v8 L={L} W={W/2} nf=1 ad='int((nf+1)/2) * W/nf * 0.29' as='int((nf+2)/2) * W/nf * 0.29'
+ pd='2*int((nf+1)/2) * (W/nf + 0.29)' ps='2*int((nf+2)/2) * (W/nf + 0.29)' nrd='0.29 / W' nrs='0.29 / W'
+ sa=0 sb=0 sd=0 mult=1 m=1
XM110 net30 net29 GND GND sky130_fd_pr__nfet_01v8 L={L} W={W/2} nf=1 ad='int((nf+1)/2) * W/nf * 0.29'
+ as='int((nf+2)/2) * W/nf * 0.29' pd='2*int((nf+1)/2) * (W/nf + 0.29)' ps='2*int((nf+2)/2) * (W/nf + 0.29)'
+ nrd='0.29 / W' nrs='0.29 / W' sa=0 sb=0 sd=0 mult=1 m=1
XM112 GND GND net28 GND sky130_fd_pr__nfet_01v8 L={L} W={W/2} nf=1 ad='int((nf+1)/2) * W/nf * 0.29' as='int((nf+2)/2) * W/nf * 0.29'
+ pd='2*int((nf+1)/2) * (W/nf + 0.29)' ps='2*int((nf+2)/2) * (W/nf + 0.29)' nrd='0.29 / W' nrs='0.29 / W'
+ sa=0 sb=0 sd=0 mult=1 m=1
XM113 GND GND GND GND sky130_fd_pr__nfet_01v8 L={L} W={W/2} nf=1 ad='int((nf+1)/2) * W/nf * 0.29' as='int((nf+2)/2) * W/nf * 0.29'
+ pd='2*int((nf+1)/2) * (W/nf + 0.29)' ps='2*int((nf+2)/2) * (W/nf + 0.29)' nrd='0.29 / W' nrs='0.29 / W'
+ sa=0 sb=0 sd=0 mult=1 m=1
XM120 net28 GND GND GND sky130_fd_pr__nfet_01v8 L={L} W={W/2} nf=1 ad='int((nf+1)/2) * W/nf * 0.29' as='int((nf+2)/2) * W/nf * 0.29'
+ pd='2*int((nf+1)/2) * (W/nf + 0.29)' ps='2*int((nf+2)/2) * (W/nf + 0.29)' nrd='0.29 / W' nrs='0.29 / W'
+ sa=0 sb=0 sd=0 mult=1 m=1
XM121 GND GND GND GND sky130_fd_pr__nfet_01v8 L={L} W={W/2} nf=1 ad='int((nf+1)/2) * W/nf * 0.29' as='int((nf+2)/2) * W/nf * 0.29'
+ pd='2*int((nf+1)/2) * (W/nf + 0.29)' ps='2*int((nf+2)/2) * (W/nf + 0.29)' nrd='0.29 / W' nrs='0.29 / W'
+ sa=0 sb=0 sd=0 mult=1 m=1
XM40 net29 net29 net30 GND sky130_fd_pr__nfet_01v8 L={L} W={W/2} nf=1 ad='int((nf+1)/2) * W/nf * 0.29'
+ as='int((nf+2)/2) * W/nf * 0.29' pd='2*int((nf+1)/2) * (W/nf + 0.29)' ps='2*int((nf+2)/2) * (W/nf + 0.29)'
+ nrd='0.29 / W' nrs='0.29 / W' sa=0 sb=0 sd=0 mult=1 m=1
XM41 net30 net29 net29 GND sky130_fd_pr__nfet_01v8 L={L} W={W/2} nf=1 ad='int((nf+1)/2) * W/nf * 0.29'
+ as='int((nf+2)/2) * W/nf * 0.29' pd='2*int((nf+1)/2) * (W/nf + 0.29)' ps='2*int((nf+2)/2) * (W/nf + 0.29)'
+ nrd='0.29 / W' nrs='0.29 / W' sa=0 sb=0 sd=0 mult=1 m=1
XM42 net29 net29 net30 GND sky130_fd_pr__nfet_01v8 L={L} W={W/2} nf=1 ad='int((nf+1)/2) * W/nf * 0.29'
+ as='int((nf+2)/2) * W/nf * 0.29' pd='2*int((nf+1)/2) * (W/nf + 0.29)' ps='2*int((nf+2)/2) * (W/nf + 0.29)'
+ nrd='0.29 / W' nrs='0.29 / W' sa=0 sb=0 sd=0 mult=1 m=1
XM43 net30 net29 net29 GND sky130_fd_pr__nfet_01v8 L={L} W={W/2} nf=1 ad='int((nf+1)/2) * W/nf * 0.29'
+ as='int((nf+2)/2) * W/nf * 0.29' pd='2*int((nf+1)/2) * (W/nf + 0.29)' ps='2*int((nf+2)/2) * (W/nf + 0.29)'
+ nrd='0.29 / W' nrs='0.29 / W' sa=0 sb=0 sd=0 mult=1 m=1
XM44 net29 net29 net30 GND sky130_fd_pr__nfet_01v8 L={L} W={W/2} nf=1 ad='int((nf+1)/2) * W/nf * 0.29'
+ as='int((nf+2)/2) * W/nf * 0.29' pd='2*int((nf+1)/2) * (W/nf + 0.29)' ps='2*int((nf+2)/2) * (W/nf + 0.29)'
+ nrd='0.29 / W' nrs='0.29 / W' sa=0 sb=0 sd=0 mult=1 m=1
XM45 net30 net29 net29 GND sky130_fd_pr__nfet_01v8 L={L} W={W/2} nf=1 ad='int((nf+1)/2) * W/nf * 0.29'
+ as='int((nf+2)/2) * W/nf * 0.29' pd='2*int((nf+1)/2) * (W/nf + 0.29)' ps='2*int((nf+2)/2) * (W/nf + 0.29)'
+ nrd='0.29 / W' nrs='0.29 / W' sa=0 sb=0 sd=0 mult=1 m=1
XM46 net29 net29 net30 GND sky130_fd_pr__nfet_01v8 L={L} W={W/2} nf=1 ad='int((nf+1)/2) * W/nf * 0.29'
+ as='int((nf+2)/2) * W/nf * 0.29' pd='2*int((nf+1)/2) * (W/nf + 0.29)' ps='2*int((nf+2)/2) * (W/nf + 0.29)'
+ nrd='0.29 / W' nrs='0.29 / W' sa=0 sb=0 sd=0 mult=1 m=1
XM102 net30 net29 net29 GND sky130_fd_pr__nfet_01v8 L={L} W={W/2} nf=1 ad='int((nf+1)/2) * W/nf * 0.29'
+ as='int((nf+2)/2) * W/nf * 0.29' pd='2*int((nf+1)/2) * (W/nf + 0.29)' ps='2*int((nf+2)/2) * (W/nf + 0.29)'
+ nrd='0.29 / W' nrs='0.29 / W' sa=0 sb=0 sd=0 mult=1 m=1
XM103 GND net29 net30 GND sky130_fd_pr__nfet_01v8 L={L} W={W/2} nf=1 ad='int((nf+1)/2) * W/nf * 0.29'
+ as='int((nf+2)/2) * W/nf * 0.29' pd='2*int((nf+1)/2) * (W/nf + 0.29)' ps='2*int((nf+2)/2) * (W/nf + 0.29)'
+ nrd='0.29 / W' nrs='0.29 / W' sa=0 sb=0 sd=0 mult=1 m=1
XM104 GND Vbn net28 GND sky130_fd_pr__nfet_01v8 L={L} W={W/2} nf=1 ad='int((nf+1)/2) * W/nf * 0.29' as='int((nf+2)/2) * W/nf * 0.29'
+ pd='2*int((nf+1)/2) * (W/nf + 0.29)' ps='2*int((nf+2)/2) * (W/nf + 0.29)' nrd='0.29 / W' nrs='0.29 / W'
+ sa=0 sb=0 sd=0 mult=1 m=1
XM105 net28 Vbn GND GND sky130_fd_pr__nfet_01v8 L={L} W={W/2} nf=1 ad='int((nf+1)/2) * W/nf * 0.29' as='int((nf+2)/2) * W/nf * 0.29'
+ pd='2*int((nf+1)/2) * (W/nf + 0.29)' ps='2*int((nf+2)/2) * (W/nf + 0.29)' nrd='0.29 / W' nrs='0.29 / W'
+ sa=0 sb=0 sd=0 mult=1 m=1
XM106 net35 net28 net36 VDD sky130_fd_pr__pfet_01v8 L={L} W={W/2} nf=1 ad='int((nf+1)/2) * W/nf * 0.29'
+ as='int((nf+2)/2) * W/nf * 0.29' pd='2*int((nf+1)/2) * (W/nf + 0.29)' ps='2*int((nf+2)/2) * (W/nf + 0.29)'
+ nrd='0.29 / W' nrs='0.29 / W' sa=0 sb=0 sd=0 mult=1 m=1
XM107 net36 net28 net37 VDD sky130_fd_pr__pfet_01v8 L={L} W={W/2} nf=1 ad='int((nf+1)/2) * W/nf * 0.29'
+ as='int((nf+2)/2) * W/nf * 0.29' pd='2*int((nf+1)/2) * (W/nf + 0.29)' ps='2*int((nf+2)/2) * (W/nf + 0.29)'
+ nrd='0.29 / W' nrs='0.29 / W' sa=0 sb=0 sd=0 mult=1 m=1
XM108 net37 net28 net38 VDD sky130_fd_pr__pfet_01v8 L={L} W={W/2} nf=1 ad='int((nf+1)/2) * W/nf * 0.29'
+ as='int((nf+2)/2) * W/nf * 0.29' pd='2*int((nf+1)/2) * (W/nf + 0.29)' ps='2*int((nf+2)/2) * (W/nf + 0.29)'
+ nrd='0.29 / W' nrs='0.29 / W' sa=0 sb=0 sd=0 mult=1 m=1
XM109 net38 net28 net29 VDD sky130_fd_pr__pfet_01v8 L={L} W={W/2} nf=1 ad='int((nf+1)/2) * W/nf * 0.29'
+ as='int((nf+2)/2) * W/nf * 0.29' pd='2*int((nf+1)/2) * (W/nf + 0.29)' ps='2*int((nf+2)/2) * (W/nf + 0.29)'
+ nrd='0.29 / W' nrs='0.29 / W' sa=0 sb=0 sd=0 mult=1 m=1
XM111 net29 net28 net34 VDD sky130_fd_pr__pfet_01v8 L={L} W={W/2} nf=1 ad='int((nf+1)/2) * W/nf * 0.29'
+ as='int((nf+2)/2) * W/nf * 0.29' pd='2*int((nf+1)/2) * (W/nf + 0.29)' ps='2*int((nf+2)/2) * (W/nf + 0.29)'
+ nrd='0.29 / W' nrs='0.29 / W' sa=0 sb=0 sd=0 mult=1 m=1
XM114 net34 net28 net33 VDD sky130_fd_pr__pfet_01v8 L={L} W={W/2} nf=1 ad='int((nf+1)/2) * W/nf * 0.29'
+ as='int((nf+2)/2) * W/nf * 0.29' pd='2*int((nf+1)/2) * (W/nf + 0.29)' ps='2*int((nf+2)/2) * (W/nf + 0.29)'
+ nrd='0.29 / W' nrs='0.29 / W' sa=0 sb=0 sd=0 mult=1 m=1
XM115 net33 net28 net32 VDD sky130_fd_pr__pfet_01v8 L={L} W={W/2} nf=1 ad='int((nf+1)/2) * W/nf * 0.29'
+ as='int((nf+2)/2) * W/nf * 0.29' pd='2*int((nf+1)/2) * (W/nf + 0.29)' ps='2*int((nf+2)/2) * (W/nf + 0.29)'
+ nrd='0.29 / W' nrs='0.29 / W' sa=0 sb=0 sd=0 mult=1 m=1
XM116 net32 net28 net31 VDD sky130_fd_pr__pfet_01v8 L={L} W={W/2} nf=1 ad='int((nf+1)/2) * W/nf * 0.29'
+ as='int((nf+2)/2) * W/nf * 0.29' pd='2*int((nf+1)/2) * (W/nf + 0.29)' ps='2*int((nf+2)/2) * (W/nf + 0.29)'
+ nrd='0.29 / W' nrs='0.29 / W' sa=0 sb=0 sd=0 mult=1 m=1
XM117 net30 GND GND GND sky130_fd_pr__nfet_01v8 L={L} W={W/2} nf=1 ad='int((nf+1)/2) * W/nf * 0.29' as='int((nf+2)/2) * W/nf * 0.29'
+ pd='2*int((nf+1)/2) * (W/nf + 0.29)' ps='2*int((nf+2)/2) * (W/nf + 0.29)' nrd='0.29 / W' nrs='0.29 / W'
+ sa=0 sb=0 sd=0 mult=1 m=1
XM118 net27 net27 net30 GND sky130_fd_pr__nfet_01v8 L={L} W={W/2} nf=1 ad='int((nf+1)/2) * W/nf * 0.29'
+ as='int((nf+2)/2) * W/nf * 0.29' pd='2*int((nf+1)/2) * (W/nf + 0.29)' ps='2*int((nf+2)/2) * (W/nf + 0.29)'
+ nrd='0.29 / W' nrs='0.29 / W' sa=0 sb=0 sd=0 mult=1 m=1
XM119 net30 net27 net27 GND sky130_fd_pr__nfet_01v8 L={L} W={W/2} nf=1 ad='int((nf+1)/2) * W/nf * 0.29'
+ as='int((nf+2)/2) * W/nf * 0.29' pd='2*int((nf+1)/2) * (W/nf + 0.29)' ps='2*int((nf+2)/2) * (W/nf + 0.29)'
+ nrd='0.29 / W' nrs='0.29 / W' sa=0 sb=0 sd=0 mult=1 m=1
XM122 GND GND net30 GND sky130_fd_pr__nfet_01v8 L={L} W={W/2} nf=1 ad='int((nf+1)/2) * W/nf * 0.29' as='int((nf+2)/2) * W/nf * 0.29'
+ pd='2*int((nf+1)/2) * (W/nf + 0.29)' ps='2*int((nf+2)/2) * (W/nf + 0.29)' nrd='0.29 / W' nrs='0.29 / W'
+ sa=0 sb=0 sd=0 mult=1 m=1
X7 GND Vbn b0out b0 mux
X9 GND Vbn b1out b1 mux
X10 GND Vbn net49 b2 mux
X11 GND Vbn net51 b3 mux
X12 GND Vbn net50 b4 mux
X13 GND Vbn net48 b5 mux
X14 GND Vbn b6out b6 mux
Vout1 net10 net46 0
.save i(vout1)
XM123 net40 net27 net39 GND sky130_fd_pr__nfet_01v8 L={L} W={W} nf=1 ad='int((nf+1)/2) * W/nf * 0.29'
+ as='int((nf+2)/2) * W/nf * 0.29' pd='2*int((nf+1)/2) * (W/nf + 0.29)' ps='2*int((nf+2)/2) * (W/nf + 0.29)'
+ nrd='0.29 / W' nrs='0.29 / W' sa=0 sb=0 sd=0 mult=1 m=1
XM124 net39 net27 net40 GND sky130_fd_pr__nfet_01v8 L={L} W={W} nf=1 ad='int((nf+1)/2) * W/nf * 0.29'
+ as='int((nf+2)/2) * W/nf * 0.29' pd='2*int((nf+1)/2) * (W/nf + 0.29)' ps='2*int((nf+2)/2) * (W/nf + 0.29)'
+ nrd='0.29 / W' nrs='0.29 / W' sa=0 sb=0 sd=0 mult=1 m=1
XM125 net40 net27 net41 GND sky130_fd_pr__nfet_01v8 L={L} W={W} nf=1 ad='int((nf+1)/2) * W/nf * 0.29'
+ as='int((nf+2)/2) * W/nf * 0.29' pd='2*int((nf+1)/2) * (W/nf + 0.29)' ps='2*int((nf+2)/2) * (W/nf + 0.29)'
+ nrd='0.29 / W' nrs='0.29 / W' sa=0 sb=0 sd=0 mult=1 m=1
XM126 net41 net27 net40 GND sky130_fd_pr__nfet_01v8 L={L} W={W} nf=1 ad='int((nf+1)/2) * W/nf * 0.29'
+ as='int((nf+2)/2) * W/nf * 0.29' pd='2*int((nf+1)/2) * (W/nf + 0.29)' ps='2*int((nf+2)/2) * (W/nf + 0.29)'
+ nrd='0.29 / W' nrs='0.29 / W' sa=0 sb=0 sd=0 mult=1 m=1
XM127 GND b0out net40 GND sky130_fd_pr__nfet_01v8 L={L} W={W} nf=1 ad='int((nf+1)/2) * W/nf * 0.29' as='int((nf+2)/2) * W/nf * 0.29'
+ pd='2*int((nf+1)/2) * (W/nf + 0.29)' ps='2*int((nf+2)/2) * (W/nf + 0.29)' nrd='0.29 / W' nrs='0.29 / W'
+ sa=0 sb=0 sd=0 mult=1 m=1
XM128 net39 b1out GND GND sky130_fd_pr__nfet_01v8 L={L} W={W} nf=1 ad='int((nf+1)/2) * W/nf * 0.29' as='int((nf+2)/2) * W/nf * 0.29'
+ pd='2*int((nf+1)/2) * (W/nf + 0.29)' ps='2*int((nf+2)/2) * (W/nf + 0.29)' nrd='0.29 / W' nrs='0.29 / W'
+ sa=0 sb=0 sd=0 mult=1 m=1
XM129 GND net48 net42 GND sky130_fd_pr__nfet_01v8 L={L} W={W} nf=1 ad='int((nf+1)/2) * W/nf * 0.29' as='int((nf+2)/2) * W/nf * 0.29'
+ pd='2*int((nf+1)/2) * (W/nf + 0.29)' ps='2*int((nf+2)/2) * (W/nf + 0.29)' nrd='0.29 / W' nrs='0.29 / W'
+ sa=0 sb=0 sd=0 mult=1 m=1
XM130 net39 net27 net43 GND sky130_fd_pr__nfet_01v8 L={L} W={W} nf=1 ad='int((nf+1)/2) * W/nf * 0.29'
+ as='int((nf+2)/2) * W/nf * 0.29' pd='2*int((nf+1)/2) * (W/nf + 0.29)' ps='2*int((nf+2)/2) * (W/nf + 0.29)'
+ nrd='0.29 / W' nrs='0.29 / W' sa=0 sb=0 sd=0 mult=1 m=1
XM131 net43 net27 net39 GND sky130_fd_pr__nfet_01v8 L={L} W={W} nf=1 ad='int((nf+1)/2) * W/nf * 0.29'
+ as='int((nf+2)/2) * W/nf * 0.29' pd='2*int((nf+1)/2) * (W/nf + 0.29)' ps='2*int((nf+2)/2) * (W/nf + 0.29)'
+ nrd='0.29 / W' nrs='0.29 / W' sa=0 sb=0 sd=0 mult=1 m=1
XM132 net39 net27 net41 GND sky130_fd_pr__nfet_01v8 L={L} W={W} nf=1 ad='int((nf+1)/2) * W/nf * 0.29'
+ as='int((nf+2)/2) * W/nf * 0.29' pd='2*int((nf+1)/2) * (W/nf + 0.29)' ps='2*int((nf+2)/2) * (W/nf + 0.29)'
+ nrd='0.29 / W' nrs='0.29 / W' sa=0 sb=0 sd=0 mult=1 m=1
XM133 net41 net27 net43 GND sky130_fd_pr__nfet_01v8 L={L} W={W} nf=1 ad='int((nf+1)/2) * W/nf * 0.29'
+ as='int((nf+2)/2) * W/nf * 0.29' pd='2*int((nf+1)/2) * (W/nf + 0.29)' ps='2*int((nf+2)/2) * (W/nf + 0.29)'
+ nrd='0.29 / W' nrs='0.29 / W' sa=0 sb=0 sd=0 mult=1 m=1
XM134 net43 net27 net44 GND sky130_fd_pr__nfet_01v8 L={L} W={W} nf=1 ad='int((nf+1)/2) * W/nf * 0.29'
+ as='int((nf+2)/2) * W/nf * 0.29' pd='2*int((nf+1)/2) * (W/nf + 0.29)' ps='2*int((nf+2)/2) * (W/nf + 0.29)'
+ nrd='0.29 / W' nrs='0.29 / W' sa=0 sb=0 sd=0 mult=1 m=1
XM135 net44 net27 net43 GND sky130_fd_pr__nfet_01v8 L={L} W={W} nf=1 ad='int((nf+1)/2) * W/nf * 0.29'
+ as='int((nf+2)/2) * W/nf * 0.29' pd='2*int((nf+1)/2) * (W/nf + 0.29)' ps='2*int((nf+2)/2) * (W/nf + 0.29)'
+ nrd='0.29 / W' nrs='0.29 / W' sa=0 sb=0 sd=0 mult=1 m=1
XM136 GND net49 net43 GND sky130_fd_pr__nfet_01v8 L={L} W={W} nf=1 ad='int((nf+1)/2) * W/nf * 0.29' as='int((nf+2)/2) * W/nf * 0.29'
+ pd='2*int((nf+1)/2) * (W/nf + 0.29)' ps='2*int((nf+2)/2) * (W/nf + 0.29)' nrd='0.29 / W' nrs='0.29 / W'
+ sa=0 sb=0 sd=0 mult=1 m=1
XM137 net45 net27 net42 GND sky130_fd_pr__nfet_01v8 L={L} W={W} nf=1 ad='int((nf+1)/2) * W/nf * 0.29'
+ as='int((nf+2)/2) * W/nf * 0.29' pd='2*int((nf+1)/2) * (W/nf + 0.29)' ps='2*int((nf+2)/2) * (W/nf + 0.29)'
+ nrd='0.29 / W' nrs='0.29 / W' sa=0 sb=0 sd=0 mult=1 m=1
XM138 net42 net27 net45 GND sky130_fd_pr__nfet_01v8 L={L} W={W} nf=1 ad='int((nf+1)/2) * W/nf * 0.29'
+ as='int((nf+2)/2) * W/nf * 0.29' pd='2*int((nf+1)/2) * (W/nf + 0.29)' ps='2*int((nf+2)/2) * (W/nf + 0.29)'
+ nrd='0.29 / W' nrs='0.29 / W' sa=0 sb=0 sd=0 mult=1 m=1
XM139 net41 net27 net42 GND sky130_fd_pr__nfet_01v8 L={L} W={W} nf=1 ad='int((nf+1)/2) * W/nf * 0.29'
+ as='int((nf+2)/2) * W/nf * 0.29' pd='2*int((nf+1)/2) * (W/nf + 0.29)' ps='2*int((nf+2)/2) * (W/nf + 0.29)'
+ nrd='0.29 / W' nrs='0.29 / W' sa=0 sb=0 sd=0 mult=1 m=1
XM140 net45 net27 net41 GND sky130_fd_pr__nfet_01v8 L={L} W={W} nf=1 ad='int((nf+1)/2) * W/nf * 0.29'
+ as='int((nf+2)/2) * W/nf * 0.29' pd='2*int((nf+1)/2) * (W/nf + 0.29)' ps='2*int((nf+2)/2) * (W/nf + 0.29)'
+ nrd='0.29 / W' nrs='0.29 / W' sa=0 sb=0 sd=0 mult=1 m=1
XM141 net44 net27 net45 GND sky130_fd_pr__nfet_01v8 L={L} W={W} nf=1 ad='int((nf+1)/2) * W/nf * 0.29'
+ as='int((nf+2)/2) * W/nf * 0.29' pd='2*int((nf+1)/2) * (W/nf + 0.29)' ps='2*int((nf+2)/2) * (W/nf + 0.29)'
+ nrd='0.29 / W' nrs='0.29 / W' sa=0 sb=0 sd=0 mult=1 m=1
XM142 net45 net27 net44 GND sky130_fd_pr__nfet_01v8 L={L} W={W} nf=1 ad='int((nf+1)/2) * W/nf * 0.29'
+ as='int((nf+2)/2) * W/nf * 0.29' pd='2*int((nf+1)/2) * (W/nf + 0.29)' ps='2*int((nf+2)/2) * (W/nf + 0.29)'
+ nrd='0.29 / W' nrs='0.29 / W' sa=0 sb=0 sd=0 mult=1 m=1
XM143 net45 net50 GND GND sky130_fd_pr__nfet_01v8 L={L} W={W} nf=1 ad='int((nf+1)/2) * W/nf * 0.29' as='int((nf+2)/2) * W/nf * 0.29'
+ pd='2*int((nf+1)/2) * (W/nf + 0.29)' ps='2*int((nf+2)/2) * (W/nf + 0.29)' nrd='0.29 / W' nrs='0.29 / W'
+ sa=0 sb=0 sd=0 mult=1 m=1
XM144 net46 net27 net47 GND sky130_fd_pr__nfet_01v8 L={L} W={W} nf=1 ad='int((nf+1)/2) * W/nf * 0.29'
+ as='int((nf+2)/2) * W/nf * 0.29' pd='2*int((nf+1)/2) * (W/nf + 0.29)' ps='2*int((nf+2)/2) * (W/nf + 0.29)'
+ nrd='0.29 / W' nrs='0.29 / W' sa=0 sb=0 sd=0 mult=1 m=1
XM145 net47 net27 net46 GND sky130_fd_pr__nfet_01v8 L={L} W={W} nf=1 ad='int((nf+1)/2) * W/nf * 0.29'
+ as='int((nf+2)/2) * W/nf * 0.29' pd='2*int((nf+1)/2) * (W/nf + 0.29)' ps='2*int((nf+2)/2) * (W/nf + 0.29)'
+ nrd='0.29 / W' nrs='0.29 / W' sa=0 sb=0 sd=0 mult=1 m=1
XM146 net42 net27 net47 GND sky130_fd_pr__nfet_01v8 L={L} W={W} nf=1 ad='int((nf+1)/2) * W/nf * 0.29'
+ as='int((nf+2)/2) * W/nf * 0.29' pd='2*int((nf+1)/2) * (W/nf + 0.29)' ps='2*int((nf+2)/2) * (W/nf + 0.29)'
+ nrd='0.29 / W' nrs='0.29 / W' sa=0 sb=0 sd=0 mult=1 m=1
XM147 net47 net27 net42 GND sky130_fd_pr__nfet_01v8 L={L} W={W} nf=1 ad='int((nf+1)/2) * W/nf * 0.29'
+ as='int((nf+2)/2) * W/nf * 0.29' pd='2*int((nf+1)/2) * (W/nf + 0.29)' ps='2*int((nf+2)/2) * (W/nf + 0.29)'
+ nrd='0.29 / W' nrs='0.29 / W' sa=0 sb=0 sd=0 mult=1 m=1
XM148 net47 b6out GND GND sky130_fd_pr__nfet_01v8 L={L} W={W} nf=1 ad='int((nf+1)/2) * W/nf * 0.29' as='int((nf+2)/2) * W/nf * 0.29'
+ pd='2*int((nf+1)/2) * (W/nf + 0.29)' ps='2*int((nf+2)/2) * (W/nf + 0.29)' nrd='0.29 / W' nrs='0.29 / W'
+ sa=0 sb=0 sd=0 mult=1 m=1
XM149 GND net51 net44 GND sky130_fd_pr__nfet_01v8 L={L} W={W} nf=1 ad='int((nf+1)/2) * W/nf * 0.29' as='int((nf+2)/2) * W/nf * 0.29'
+ pd='2*int((nf+1)/2) * (W/nf + 0.29)' ps='2*int((nf+2)/2) * (W/nf + 0.29)' nrd='0.29 / W' nrs='0.29 / W'
+ sa=0 sb=0 sd=0 mult=1 m=1
XM150 net41 net27 net44 GND sky130_fd_pr__nfet_01v8 L={L} W={W} nf=1 ad='int((nf+1)/2) * W/nf * 0.29'
+ as='int((nf+2)/2) * W/nf * 0.29' pd='2*int((nf+1)/2) * (W/nf + 0.29)' ps='2*int((nf+2)/2) * (W/nf + 0.29)'
+ nrd='0.29 / W' nrs='0.29 / W' sa=0 sb=0 sd=0 mult=1 m=1
XM151 VDD net41 net41 VDD sky130_fd_pr__pfet_01v8 L={L} W={W} nf=1 ad='int((nf+1)/2) * W/nf * 0.29' as='int((nf+2)/2) * W/nf * 0.29'
+ pd='2*int((nf+1)/2) * (W/nf + 0.29)' ps='2*int((nf+2)/2) * (W/nf + 0.29)' nrd='0.29 / W' nrs='0.29 / W'
+ sa=0 sb=0 sd=0 mult=1 m=1
**** begin user architecture code

.param W=24
.param L=1
.control
set wr_vecnames
set wr_singlescale
let code = 0
  while code < 128
    if code eq 0
      let b0 = 0
    else
      let b0 = code % 2 * 1.8
    end
    if floor(code / 2) eq 0
      let b1 = 0
    else
      let b1 = floor(code / 2) % 2 * 1.8
    end
    if floor(code / 4) eq 0
      let b2 = 0
    else
      let b2 = floor(code / 4) % 2 * 1.8
    end
    if floor(code / 8) eq 0
      let b3 = 0
    else
      let b3 = floor(code / 8) % 2 * 1.8
    end
    if floor(code / 16) eq 0
      let b4 = 0
    else
      let b4 = floor(code / 16) % 2 * 1.8
    end
    if floor(code / 32) eq 0
      let b5 = 0
    else
      let b5 = floor(code / 32) % 2 * 1.8
    end
    if floor(code / 64) eq 0
      let b6 = 0
    else
      let b6 = floor(code / 64) % 2 * 1.8
    end
    alter v0 $&b0
    alter v1 $&b1
    alter v2 $&b2
    alter v3 $&b3
    alter v4 $&b4
    alter v5 $&b5
    alter v6 $&b6
    save all
    op
    wrdata ~/Documents/current-output-dac-vlsi/simulations/dac_sim.txt v(Vbn) i(Vout) i(Vout1) v(b6)
+ v(b5) v(b4) v(b3) v(b2) v(b1) v(b0) v(b0out) v(b1out) v(b6out)
    if code eq 0
      set appendwrite
      set wr_vecnames = FALSE
    end
    let code = code + 1
  end
.endc


.option wnflag=1
.param MC_SWITCH=0.0
.lib ~/skywater/skywater-pdk/libraries/sky130_fd_pr_ngspice/latest/models/sky130.lib.spice tt

**** end user architecture code
**.ends

* expanding   symbol:  /home/madvlsi/Documents/current-output-dac-vlsi/schematics/mux.sym # of
*+ pins=4
** sym_path: /home/madvlsi/Documents/current-output-dac-vlsi/schematics/mux.sym
** sch_path: /home/madvlsi/Documents/current-output-dac-vlsi/schematics/mux.sch
.subckt mux A B Y S
*.ipin S
*.ipin A
*.opin Y
*.ipin B
XM1 net1 S GND GND sky130_fd_pr__nfet_01v8 L=0.15 W=1 nf=1 ad='int((nf+1)/2) * W/nf * 0.29' as='int((nf+2)/2) * W/nf * 0.29'
+ pd='2*int((nf+1)/2) * (W/nf + 0.29)' ps='2*int((nf+2)/2) * (W/nf + 0.29)' nrd='0.29 / W' nrs='0.29 / W'
+ sa=0 sb=0 sd=0 mult=1 m=1
XM2 net1 S VDD VDD sky130_fd_pr__pfet_01v8 L=0.15 W=1 nf=1 ad='int((nf+1)/2) * W/nf * 0.29' as='int((nf+2)/2) * W/nf * 0.29'
+ pd='2*int((nf+1)/2) * (W/nf + 0.29)' ps='2*int((nf+2)/2) * (W/nf + 0.29)' nrd='0.29 / W' nrs='0.29 / W'
+ sa=0 sb=0 sd=0 mult=1 m=1
XM3 Y S B GND sky130_fd_pr__nfet_01v8 L=0.15 W=1 nf=1 ad='int((nf+1)/2) * W/nf * 0.29' as='int((nf+2)/2) * W/nf * 0.29'
+ pd='2*int((nf+1)/2) * (W/nf + 0.29)' ps='2*int((nf+2)/2) * (W/nf + 0.29)' nrd='0.29 / W' nrs='0.29 / W'
+ sa=0 sb=0 sd=0 mult=1 m=1
XM4 A net1 Y GND sky130_fd_pr__nfet_01v8 L=0.15 W=1 nf=1 ad='int((nf+1)/2) * W/nf * 0.29' as='int((nf+2)/2) * W/nf * 0.29'
+ pd='2*int((nf+1)/2) * (W/nf + 0.29)' ps='2*int((nf+2)/2) * (W/nf + 0.29)' nrd='0.29 / W' nrs='0.29 / W'
+ sa=0 sb=0 sd=0 mult=1 m=1
.ends

.GLOBAL GND
.GLOBAL VDD
.end
